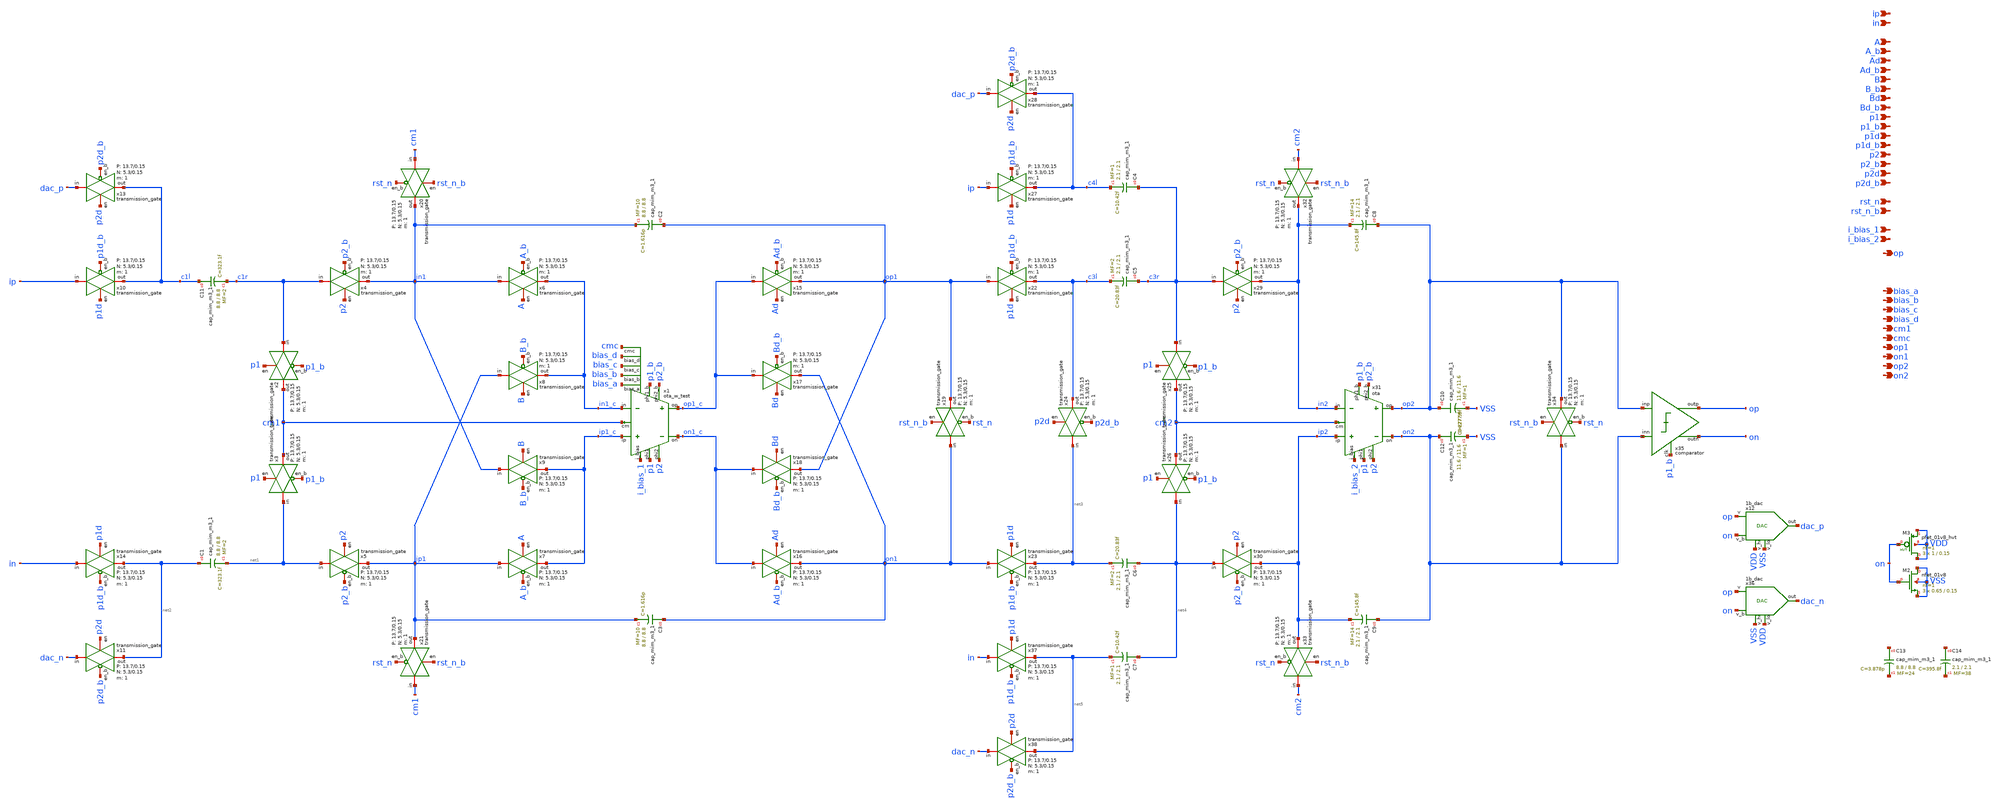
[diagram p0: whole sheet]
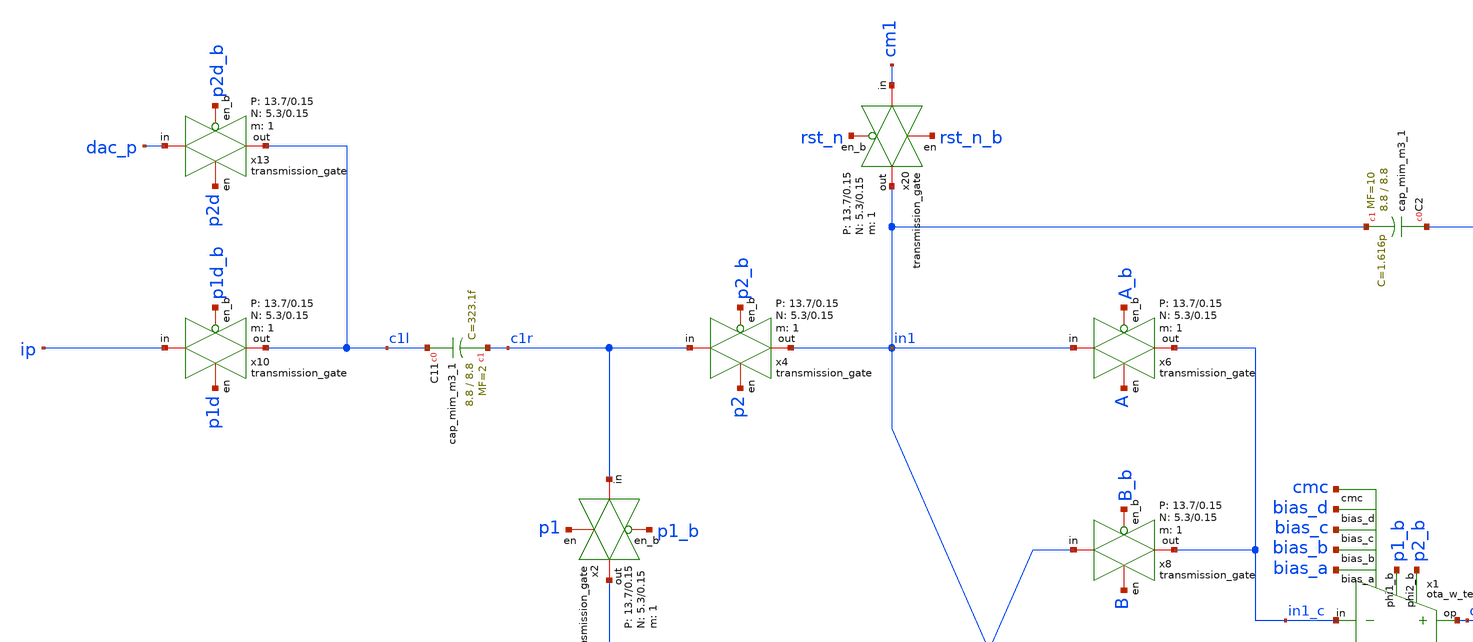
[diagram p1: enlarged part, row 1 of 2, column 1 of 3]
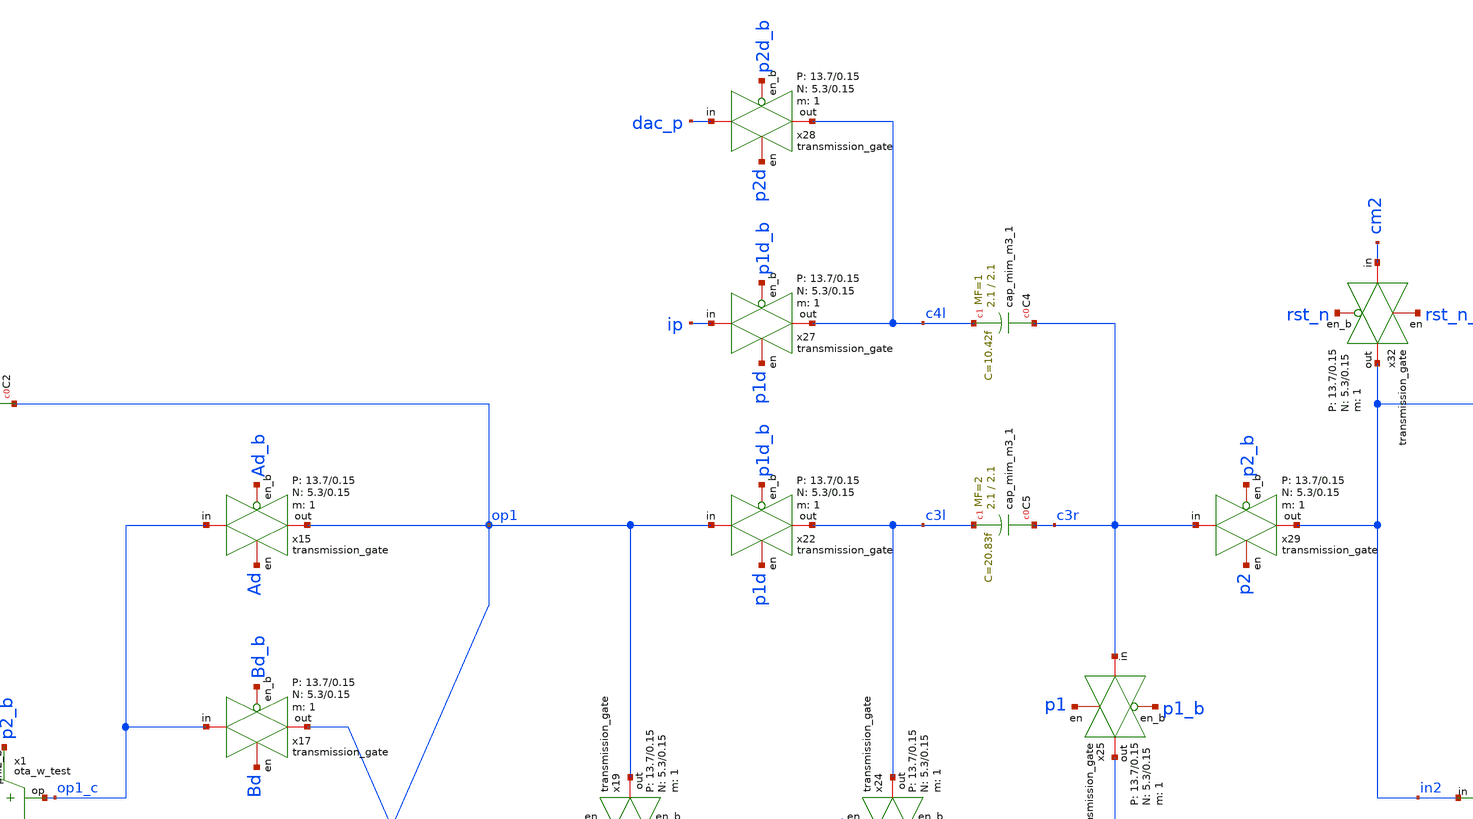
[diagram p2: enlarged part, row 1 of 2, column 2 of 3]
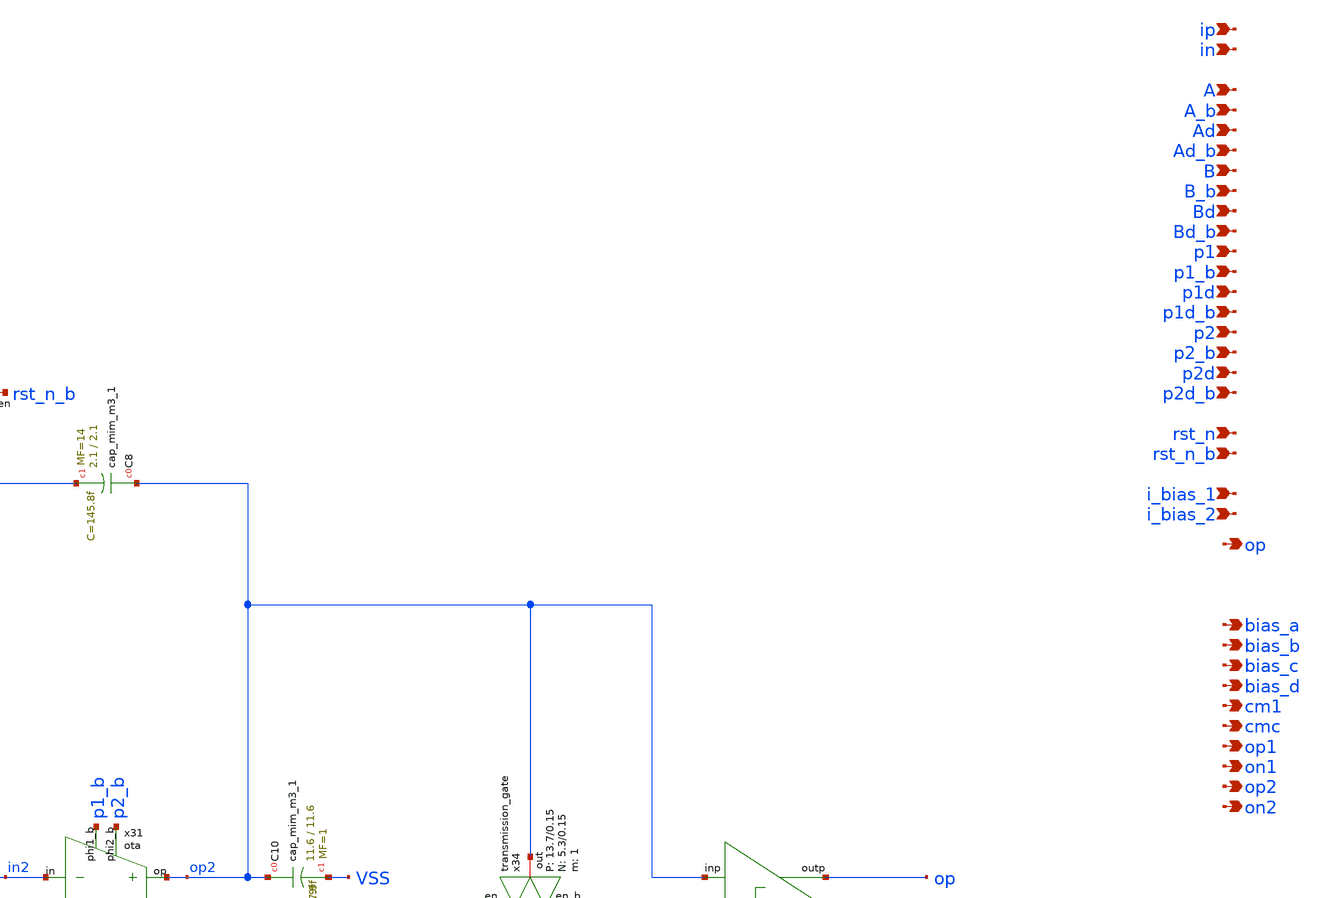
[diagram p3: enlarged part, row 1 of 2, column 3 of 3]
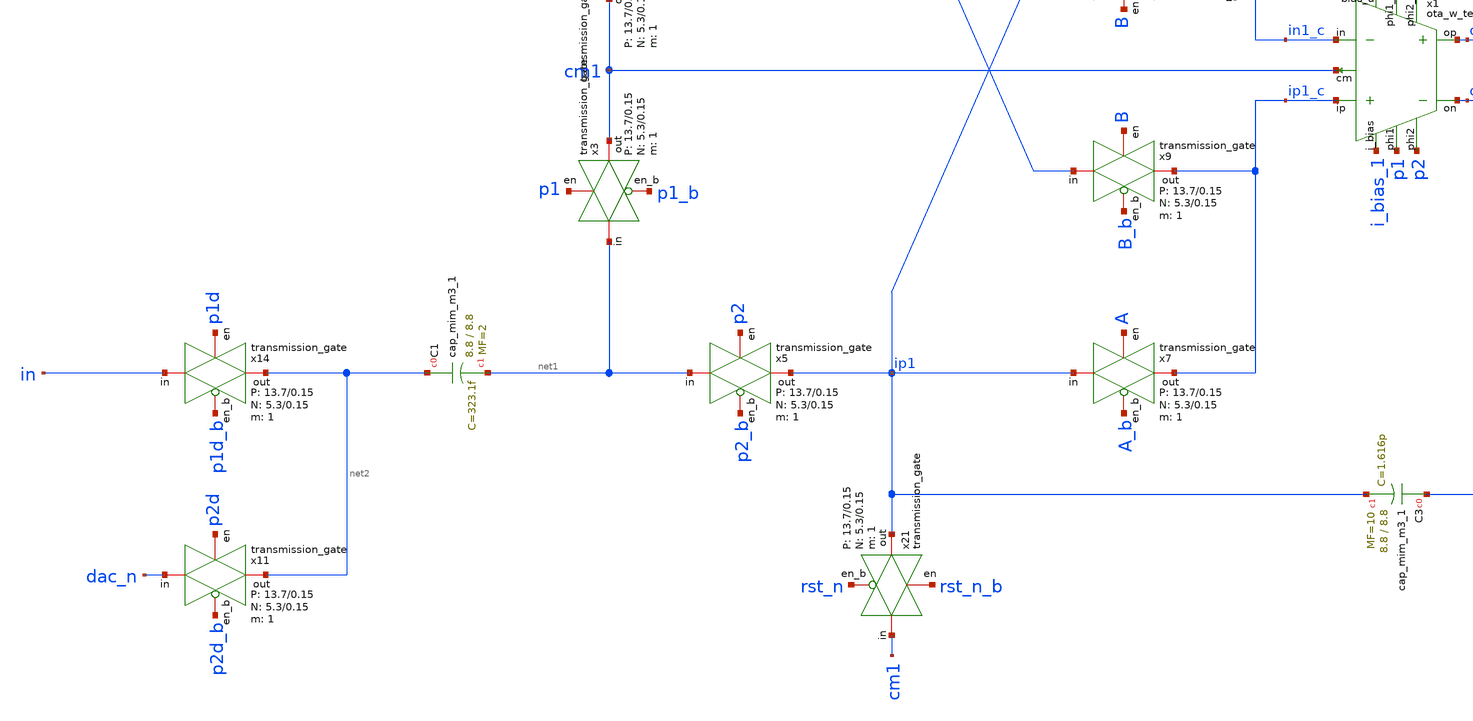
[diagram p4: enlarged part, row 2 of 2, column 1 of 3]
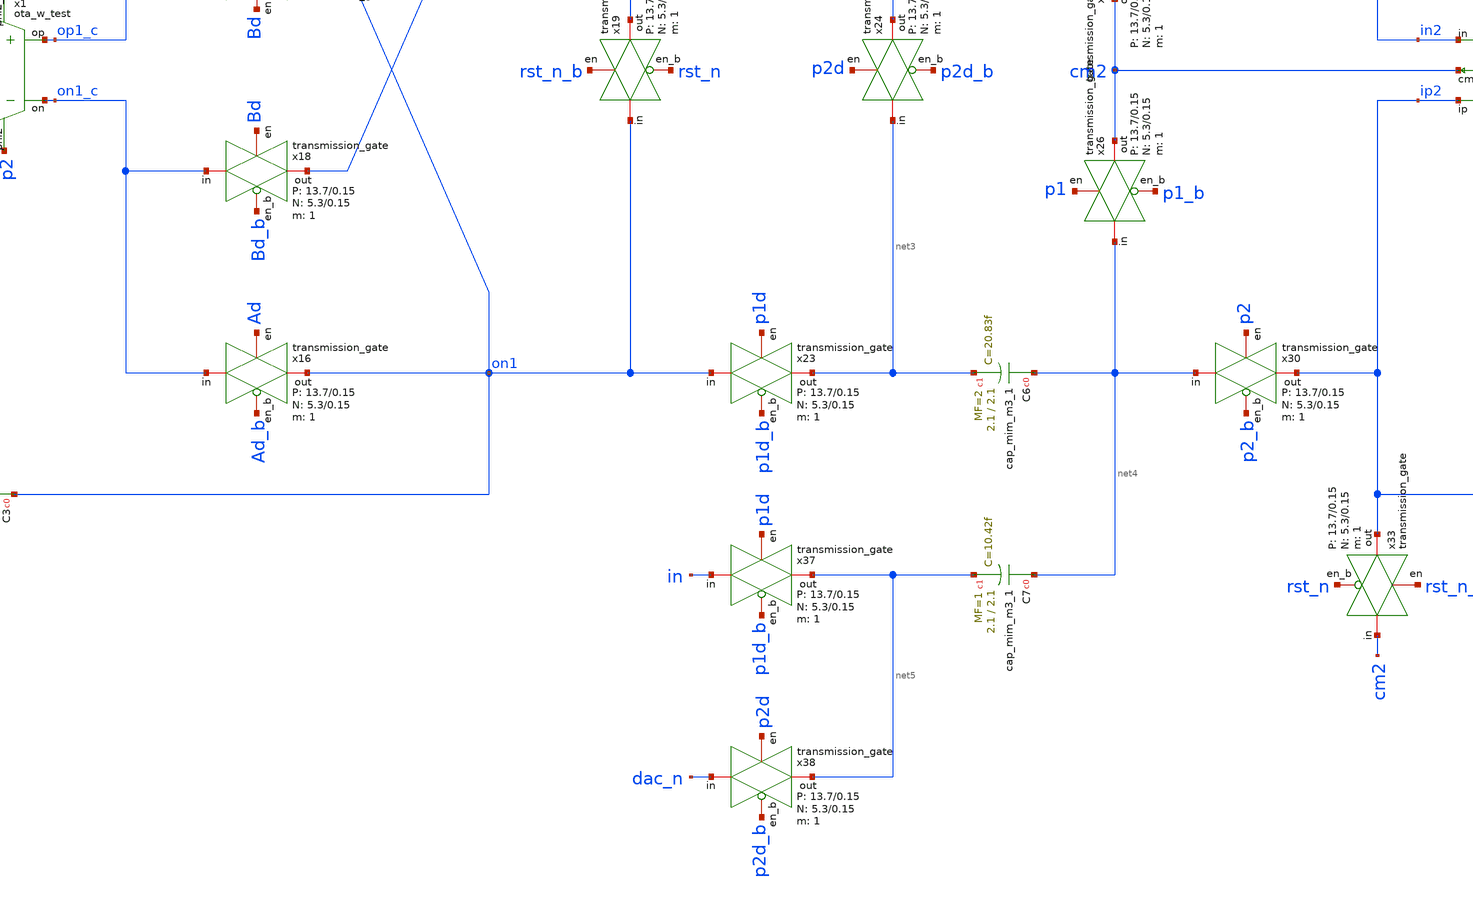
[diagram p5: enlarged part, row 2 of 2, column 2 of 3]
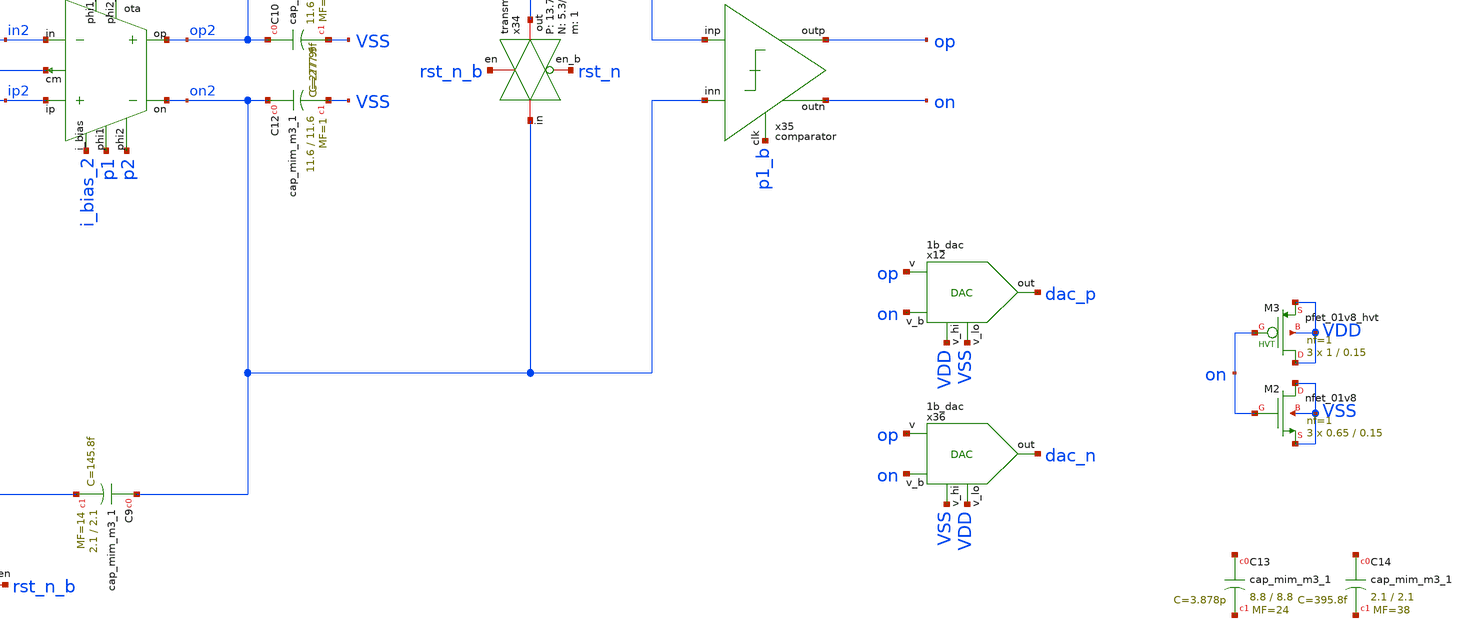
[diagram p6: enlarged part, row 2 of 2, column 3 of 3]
** sch_path: design/analog_modulator/schematic/modulator_w_test.sch
**.subckt modulator_w_test ip in A A_b Ad Ad_b B B_b Bd Bd_b p1 p1_b p1d p1d_b p2 p2_b p2d p2d_b
*+ rst_n rst_n_b i_bias_1 i_bias_2 op bias_a bias_b bias_c bias_d cm1 cmc op1 on1 op2 on2
*.ipin ip
*.ipin in
*.ipin A
*.ipin A_b
*.ipin Ad
*.ipin Ad_b
*.ipin B
*.ipin B_b
*.ipin Bd
*.ipin Bd_b
*.ipin p1
*.ipin p1_b
*.ipin p1d
*.ipin p1d_b
*.ipin p2
*.ipin p2_b
*.ipin p2d
*.ipin p2d_b
*.ipin rst_n
*.ipin rst_n_b
*.ipin i_bias_1
*.ipin i_bias_2
*.opin op
*.opin bias_a
*.opin bias_b
*.opin bias_c
*.opin bias_d
*.opin cm1
*.opin cmc
*.opin op1
*.opin on1
*.opin op2
*.opin on2
x4 c1r in1 p2 p2_b VDD VSS 1 5.3 0.15 13.7 0.15 transmission_gate
x5 net1 ip1 p2 p2_b VDD VSS 1 5.3 0.15 13.7 0.15 transmission_gate
x2 c1r cm1 p1 p1_b VDD VSS 1 5.3 0.15 13.7 0.15 transmission_gate
x3 net1 cm1 p1 p1_b VDD VSS 1 5.3 0.15 13.7 0.15 transmission_gate
x10 ip c1l p1d p1d_b VDD VSS 1 5.3 0.15 13.7 0.15 transmission_gate
x11 dac_n net2 p2d p2d_b VDD VSS 1 5.3 0.15 13.7 0.15 transmission_gate
x12 VDD VSS op dac_p on VDD VSS 1b_dac
x13 dac_p c1l p2d p2d_b VDD VSS 1 5.3 0.15 13.7 0.15 transmission_gate
x14 in net2 p1d p1d_b VDD VSS 1 5.3 0.15 13.7 0.15 transmission_gate
x19 on1 op1 rst_n_b rst_n VDD VSS 1 5.3 0.15 13.7 0.15 transmission_gate
x20 cm1 in1 rst_n_b rst_n VDD VSS 1 5.3 0.15 13.7 0.15 transmission_gate
x21 cm1 ip1 rst_n_b rst_n VDD VSS 1 5.3 0.15 13.7 0.15 transmission_gate
x22 op1 c3l p1d p1d_b VDD VSS 1 5.3 0.15 13.7 0.15 transmission_gate
x23 on1 net3 p1d p1d_b VDD VSS 1 5.3 0.15 13.7 0.15 transmission_gate
x24 net3 c3l p2d p2d_b VDD VSS 1 5.3 0.15 13.7 0.15 transmission_gate
x25 c3r cm2 p1 p1_b VDD VSS 1 5.3 0.15 13.7 0.15 transmission_gate
x26 net4 cm2 p1 p1_b VDD VSS 1 5.3 0.15 13.7 0.15 transmission_gate
x27 ip c4l p1d p1d_b VDD VSS 1 5.3 0.15 13.7 0.15 transmission_gate
x28 dac_p c4l p2d p2d_b VDD VSS 1 5.3 0.15 13.7 0.15 transmission_gate
x29 c3r in2 p2 p2_b VDD VSS 1 5.3 0.15 13.7 0.15 transmission_gate
x30 net4 ip2 p2 p2_b VDD VSS 1 5.3 0.15 13.7 0.15 transmission_gate
x32 cm2 in2 rst_n_b rst_n VDD VSS 1 5.3 0.15 13.7 0.15 transmission_gate
x33 cm2 ip2 rst_n_b rst_n VDD VSS 1 5.3 0.15 13.7 0.15 transmission_gate
x34 on2 op2 rst_n_b rst_n VDD VSS 1 5.3 0.15 13.7 0.15 transmission_gate
x36 VSS VDD op dac_n on VDD VSS 1b_dac
x37 in net5 p1d p1d_b VDD VSS 1 5.3 0.15 13.7 0.15 transmission_gate
x38 dac_n net5 p2d p2d_b VDD VSS 1 5.3 0.15 13.7 0.15 transmission_gate
XC11 c1l c1r sky130_fd_pr__cap_mim_m3_1 W=8.8 L=8.8 MF=2 m=2
XC1 net2 net1 sky130_fd_pr__cap_mim_m3_1 W=8.8 L=8.8 MF=2 m=2
XC2 op1 in1 sky130_fd_pr__cap_mim_m3_1 W=8.8 L=8.8 MF=10 m=10
XC3 on1 ip1 sky130_fd_pr__cap_mim_m3_1 W=8.8 L=8.8 MF=10 m=10
XC4 c3r c4l sky130_fd_pr__cap_mim_m3_1 W=2.1 L=2.1 MF=1 m=1
XC5 c3r c3l sky130_fd_pr__cap_mim_m3_1 W=2.1 L=2.1 MF=2 m=2
XC6 net4 net3 sky130_fd_pr__cap_mim_m3_1 W=2.1 L=2.1 MF=2 m=2
XC7 net4 net5 sky130_fd_pr__cap_mim_m3_1 W=2.1 L=2.1 MF=1 m=1
XC8 op2 in2 sky130_fd_pr__cap_mim_m3_1 W=2.1 L=2.1 MF=14 m=14
XC9 on2 ip2 sky130_fd_pr__cap_mim_m3_1 W=2.1 L=2.1 MF=14 m=14
XC10 op2 VSS sky130_fd_pr__cap_mim_m3_1 W=11.6 L=11.6 MF=1 m=1
XC12 on2 VSS sky130_fd_pr__cap_mim_m3_1 W=11.6 L=11.6 MF=1 m=1
x6 in1 in1_c A A_b VDD VSS 1 5.3 0.15 13.7 0.15 transmission_gate
x8 ip1 in1_c B B_b VDD VSS 1 5.3 0.15 13.7 0.15 transmission_gate
x15 op1_c op1 Ad Ad_b VDD VSS 1 5.3 0.15 13.7 0.15 transmission_gate
x16 on1_c on1 Ad Ad_b VDD VSS 1 5.3 0.15 13.7 0.15 transmission_gate
x17 op1_c on1 Bd Bd_b VDD VSS 1 5.3 0.15 13.7 0.15 transmission_gate
x18 on1_c op1 Bd Bd_b VDD VSS 1 5.3 0.15 13.7 0.15 transmission_gate
x7 ip1 ip1_c A A_b VDD VSS 1 5.3 0.15 13.7 0.15 transmission_gate
x9 in1 ip1_c B B_b VDD VSS 1 5.3 0.15 13.7 0.15 transmission_gate
XC13 net6 net7 sky130_fd_pr__cap_mim_m3_1 W=8.8 L=8.8 MF=24 m=24
XC14 net8 net9 sky130_fd_pr__cap_mim_m3_1 W=2.1 L=2.1 MF=38 m=38
x35 op2 on2 op p1_b on VDD VSS comparator
XM2 VSS on VSS VSS sky130_fd_pr__nfet_01v8 L=0.15 W=0.65 nf=1 ad='int((nf+1)/2) * W/nf * 0.29' as='int((nf+2)/2) * W/nf * 0.29'
+ pd='2*int((nf+1)/2) * (W/nf + 0.29)' ps='2*int((nf+2)/2) * (W/nf + 0.29)' nrd='0.29 / W' nrs='0.29 / W'
+ sa=0 sb=0 sd=0 mult=3 m=3
XM3 VDD on VDD VDD sky130_fd_pr__pfet_01v8_hvt L=0.15 W=1 nf=1 ad='int((nf+1)/2) * W/nf * 0.29' as='int((nf+2)/2) * W/nf * 0.29'
+ pd='2*int((nf+1)/2) * (W/nf + 0.29)' ps='2*int((nf+2)/2) * (W/nf + 0.29)' nrd='0.29 / W' nrs='0.29 / W'
+ sa=0 sb=0 sd=0 mult=3 m=3
x1 i_bias_1 ip1_c in1_c p1 p1_b p2 p2_b op1_c on1_c cm1 bias_a bias_b bias_c bias_d cmc VDD VSS
+ ota_w_test
x31 i_bias_2 ip2 in2 p1 p1_b p2 p2_b op2 on2 cm2 VDD VSS ota
**.ends
.end
